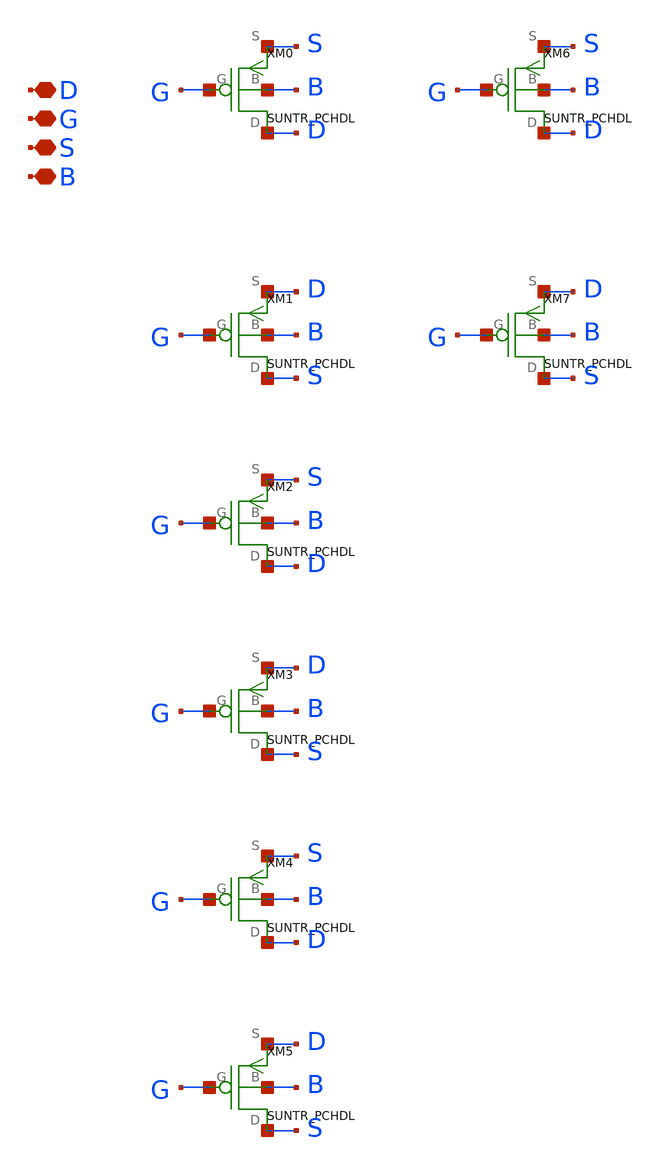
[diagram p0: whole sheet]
** sch_path: ip/sun_tr_sky130nm/design/SUN_TR_SKY130NM/SUNTR_PCHDLA.sch
**.subckt SUNTR_PCHDLA D G S B
*.iopin D
*.iopin G
*.iopin S
*.iopin B
XM0 D G S B SUNTR_PCHDL
XM1 S G D B SUNTR_PCHDL
XM2 D G S B SUNTR_PCHDL
XM3 S G D B SUNTR_PCHDL
XM4 D G S B SUNTR_PCHDL
XM5 S G D B SUNTR_PCHDL
XM6 D G S B SUNTR_PCHDL
XM7 S G D B SUNTR_PCHDL
**.ends
.end
